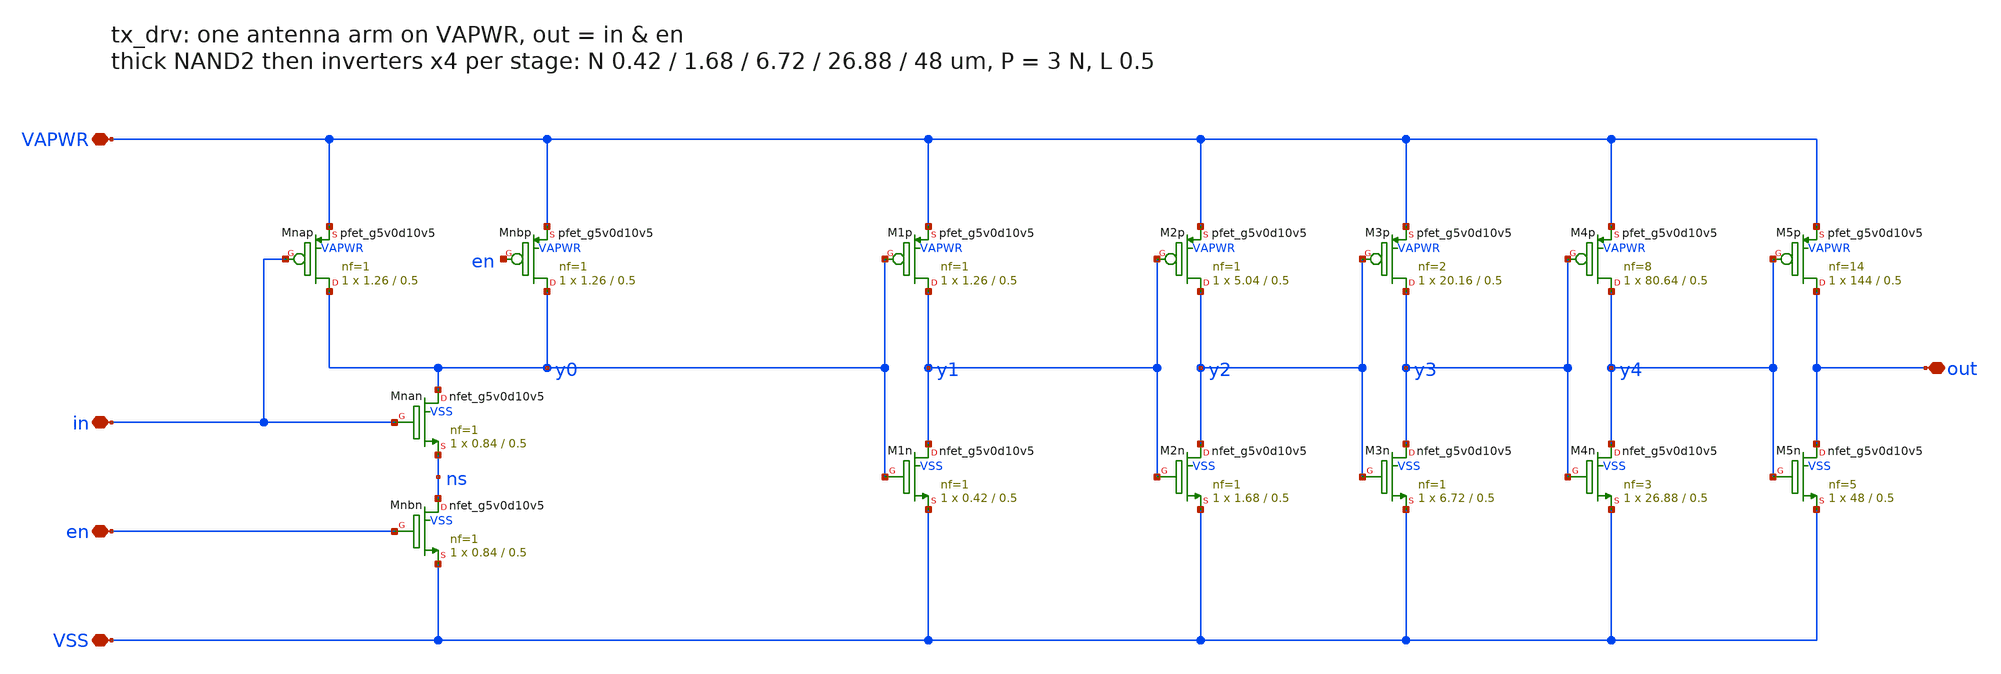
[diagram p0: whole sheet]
** sch_path: xschem/tx_drv.sch
**.subckt tx_drv VAPWR VSS in en out
*.iopin VAPWR
*.iopin VSS
*.iopin in
*.iopin en
*.iopin out
XMnap y0 in VAPWR VAPWR sky130_fd_pr__pfet_g5v0d10v5 L=0.5 W=1.26 nf=1 ad='int((nf+1)/2) * W/nf * 0.29'
+ as='int((nf+2)/2) * W/nf * 0.29' pd='2*int((nf+1)/2) * (W/nf + 0.29)' ps='2*int((nf+2)/2) * (W/nf + 0.29)'
+ nrd='0.29 / W' nrs='0.29 / W' sa=0 sb=0 sd=0 mult=1 m=1
XMnbp y0 en VAPWR VAPWR sky130_fd_pr__pfet_g5v0d10v5 L=0.5 W=1.26 nf=1 ad='int((nf+1)/2) * W/nf * 0.29'
+ as='int((nf+2)/2) * W/nf * 0.29' pd='2*int((nf+1)/2) * (W/nf + 0.29)' ps='2*int((nf+2)/2) * (W/nf + 0.29)'
+ nrd='0.29 / W' nrs='0.29 / W' sa=0 sb=0 sd=0 mult=1 m=1
XMnan y0 in ns VSS sky130_fd_pr__nfet_g5v0d10v5 L=0.5 W=0.84 nf=1 ad='int((nf+1)/2) * W/nf * 0.29' as='int((nf+2)/2) * W/nf * 0.29'
+ pd='2*int((nf+1)/2) * (W/nf + 0.29)' ps='2*int((nf+2)/2) * (W/nf + 0.29)' nrd='0.29 / W' nrs='0.29 / W'
+ sa=0 sb=0 sd=0 mult=1 m=1
XMnbn ns en VSS VSS sky130_fd_pr__nfet_g5v0d10v5 L=0.5 W=0.84 nf=1 ad='int((nf+1)/2) * W/nf * 0.29' as='int((nf+2)/2) * W/nf * 0.29'
+ pd='2*int((nf+1)/2) * (W/nf + 0.29)' ps='2*int((nf+2)/2) * (W/nf + 0.29)' nrd='0.29 / W' nrs='0.29 / W'
+ sa=0 sb=0 sd=0 mult=1 m=1
XM1p y1 y0 VAPWR VAPWR sky130_fd_pr__pfet_g5v0d10v5 L=0.5 W=1.26 nf=1 ad='int((nf+1)/2) * W/nf * 0.29'
+ as='int((nf+2)/2) * W/nf * 0.29' pd='2*int((nf+1)/2) * (W/nf + 0.29)' ps='2*int((nf+2)/2) * (W/nf + 0.29)'
+ nrd='0.29 / W' nrs='0.29 / W' sa=0 sb=0 sd=0 mult=1 m=1
XM1n y1 y0 VSS VSS sky130_fd_pr__nfet_g5v0d10v5 L=0.5 W=0.42 nf=1 ad='int((nf+1)/2) * W/nf * 0.29' as='int((nf+2)/2) * W/nf * 0.29'
+ pd='2*int((nf+1)/2) * (W/nf + 0.29)' ps='2*int((nf+2)/2) * (W/nf + 0.29)' nrd='0.29 / W' nrs='0.29 / W'
+ sa=0 sb=0 sd=0 mult=1 m=1
XM2p y2 y1 VAPWR VAPWR sky130_fd_pr__pfet_g5v0d10v5 L=0.5 W=5.04 nf=1 ad='int((nf+1)/2) * W/nf * 0.29'
+ as='int((nf+2)/2) * W/nf * 0.29' pd='2*int((nf+1)/2) * (W/nf + 0.29)' ps='2*int((nf+2)/2) * (W/nf + 0.29)'
+ nrd='0.29 / W' nrs='0.29 / W' sa=0 sb=0 sd=0 mult=1 m=1
XM2n y2 y1 VSS VSS sky130_fd_pr__nfet_g5v0d10v5 L=0.5 W=1.68 nf=1 ad='int((nf+1)/2) * W/nf * 0.29' as='int((nf+2)/2) * W/nf * 0.29'
+ pd='2*int((nf+1)/2) * (W/nf + 0.29)' ps='2*int((nf+2)/2) * (W/nf + 0.29)' nrd='0.29 / W' nrs='0.29 / W'
+ sa=0 sb=0 sd=0 mult=1 m=1
XM3p y3 y2 VAPWR VAPWR sky130_fd_pr__pfet_g5v0d10v5 L=0.5 W=20.16 nf=2 ad='int((nf+1)/2) * W/nf * 0.29'
+ as='int((nf+2)/2) * W/nf * 0.29' pd='2*int((nf+1)/2) * (W/nf + 0.29)' ps='2*int((nf+2)/2) * (W/nf + 0.29)'
+ nrd='0.29 / W' nrs='0.29 / W' sa=0 sb=0 sd=0 mult=1 m=1
XM3n y3 y2 VSS VSS sky130_fd_pr__nfet_g5v0d10v5 L=0.5 W=6.72 nf=1 ad='int((nf+1)/2) * W/nf * 0.29' as='int((nf+2)/2) * W/nf * 0.29'
+ pd='2*int((nf+1)/2) * (W/nf + 0.29)' ps='2*int((nf+2)/2) * (W/nf + 0.29)' nrd='0.29 / W' nrs='0.29 / W'
+ sa=0 sb=0 sd=0 mult=1 m=1
XM4p y4 y3 VAPWR VAPWR sky130_fd_pr__pfet_g5v0d10v5 L=0.5 W=80.64 nf=8 ad='int((nf+1)/2) * W/nf * 0.29'
+ as='int((nf+2)/2) * W/nf * 0.29' pd='2*int((nf+1)/2) * (W/nf + 0.29)' ps='2*int((nf+2)/2) * (W/nf + 0.29)'
+ nrd='0.29 / W' nrs='0.29 / W' sa=0 sb=0 sd=0 mult=1 m=1
XM4n y4 y3 VSS VSS sky130_fd_pr__nfet_g5v0d10v5 L=0.5 W=26.88 nf=3 ad='int((nf+1)/2) * W/nf * 0.29' as='int((nf+2)/2) * W/nf * 0.29'
+ pd='2*int((nf+1)/2) * (W/nf + 0.29)' ps='2*int((nf+2)/2) * (W/nf + 0.29)' nrd='0.29 / W' nrs='0.29 / W'
+ sa=0 sb=0 sd=0 mult=1 m=1
XM5p out y4 VAPWR VAPWR sky130_fd_pr__pfet_g5v0d10v5 L=0.5 W=144 nf=14 ad='int((nf+1)/2) * W/nf * 0.29'
+ as='int((nf+2)/2) * W/nf * 0.29' pd='2*int((nf+1)/2) * (W/nf + 0.29)' ps='2*int((nf+2)/2) * (W/nf + 0.29)'
+ nrd='0.29 / W' nrs='0.29 / W' sa=0 sb=0 sd=0 mult=1 m=1
XM5n out y4 VSS VSS sky130_fd_pr__nfet_g5v0d10v5 L=0.5 W=48 nf=5 ad='int((nf+1)/2) * W/nf * 0.29' as='int((nf+2)/2) * W/nf * 0.29'
+ pd='2*int((nf+1)/2) * (W/nf + 0.29)' ps='2*int((nf+2)/2) * (W/nf + 0.29)' nrd='0.29 / W' nrs='0.29 / W'
+ sa=0 sb=0 sd=0 mult=1 m=1
**.ends
.end
